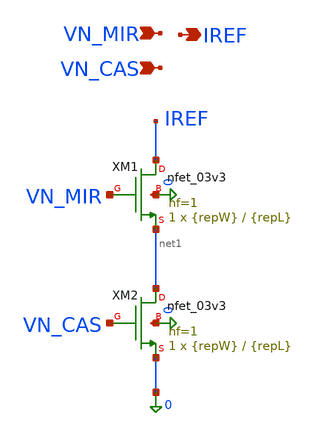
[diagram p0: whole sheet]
** sch_path: blocks/dac/iref/dac_mirror.sch
**.subckt dac_mirror VN_MIR IREF VN_CAS
*.ipin VN_MIR
*.opin IREF
*.ipin VN_CAS
XM1 IREF VN_MIR net1 0 nfet_03v3 L={repL} W={repW} nf=1 ad='int((nf+1)/2) * W/nf * 0.18u' as='int((nf+2)/2) * W/nf * 0.18u'
+ pd='2*int((nf+1)/2) * (W/nf + 0.18u)' ps='2*int((nf+2)/2) * (W/nf + 0.18u)' nrd='0.18u / W' nrs='0.18u / W'
+ sa=0 sb=0 sd=0 m=1
XM2 net1 VN_CAS 0 0 nfet_03v3 L={repL} W={repW} nf=1 ad='int((nf+1)/2) * W/nf * 0.18u' as='int((nf+2)/2) * W/nf * 0.18u'
+ pd='2*int((nf+1)/2) * (W/nf + 0.18u)' ps='2*int((nf+2)/2) * (W/nf + 0.18u)' nrd='0.18u / W' nrs='0.18u / W'
+ sa=0 sb=0 sd=0 m=1
**.ends
.end
